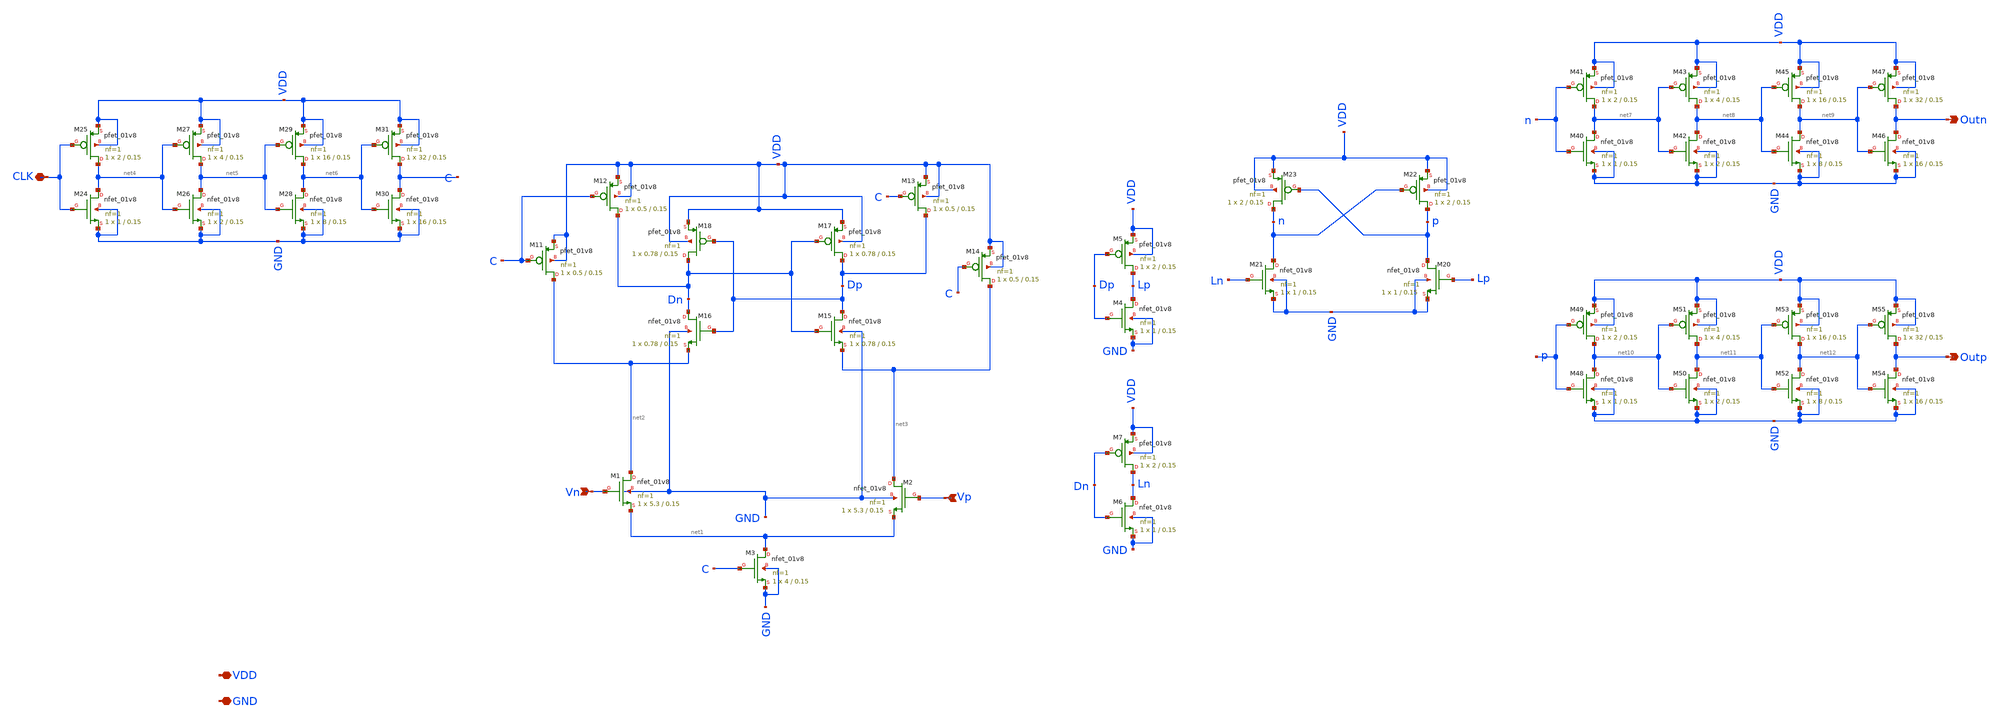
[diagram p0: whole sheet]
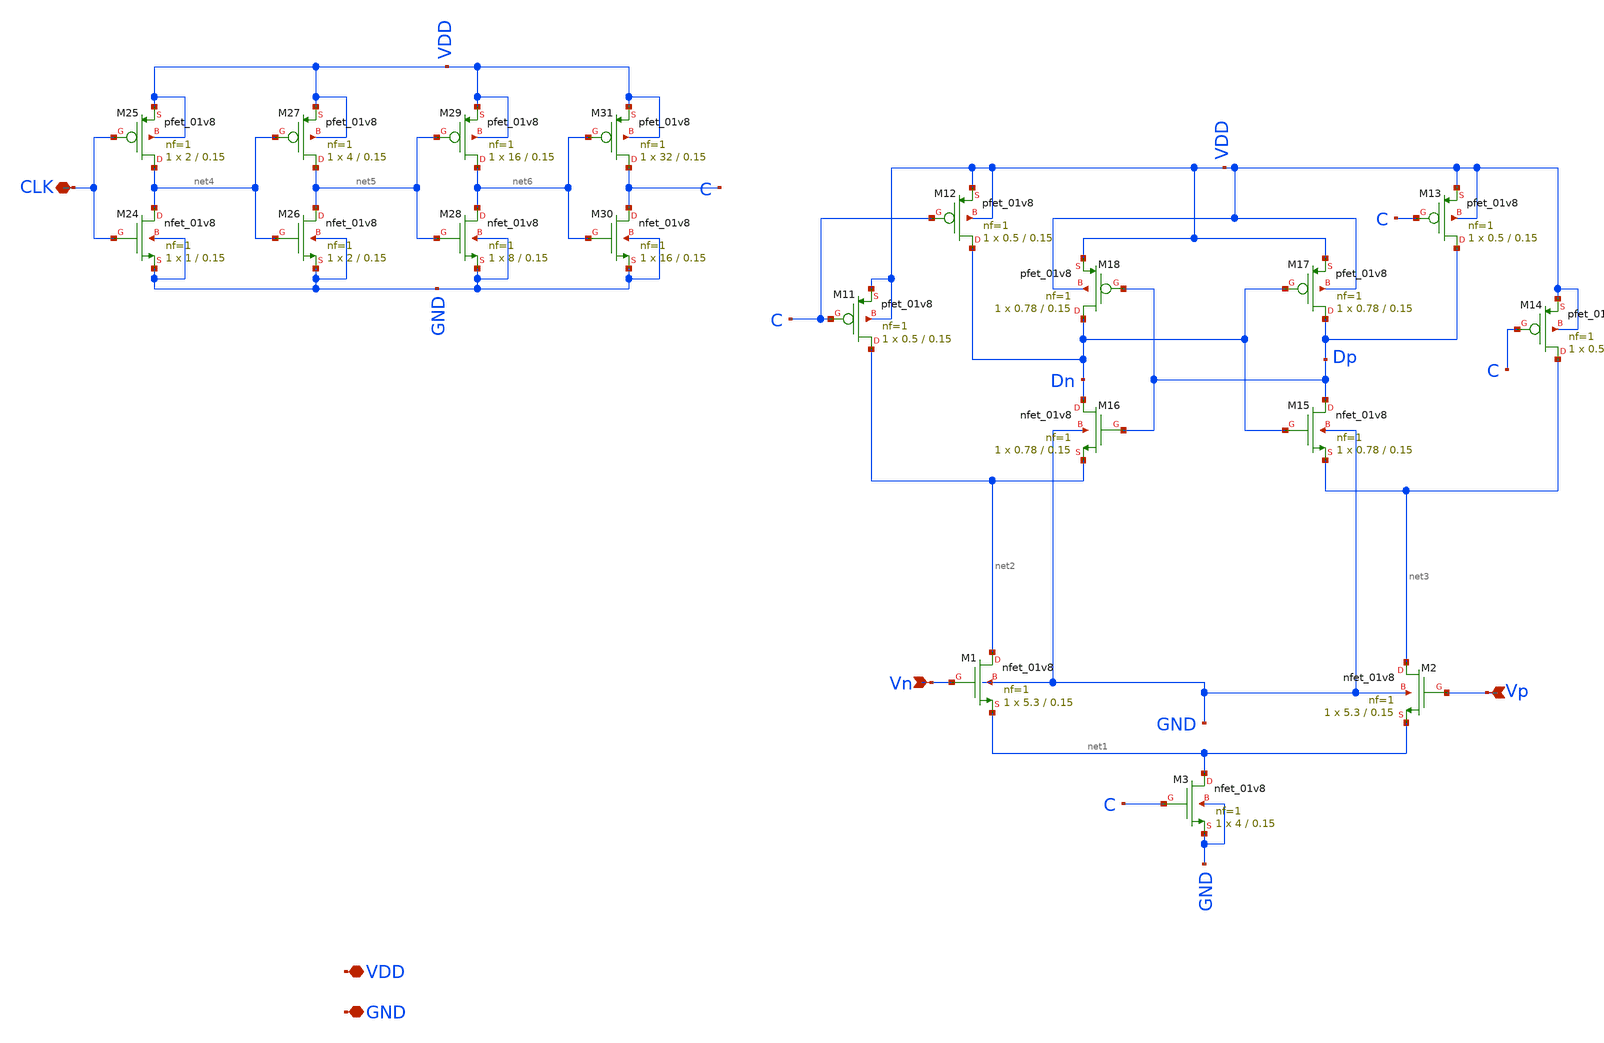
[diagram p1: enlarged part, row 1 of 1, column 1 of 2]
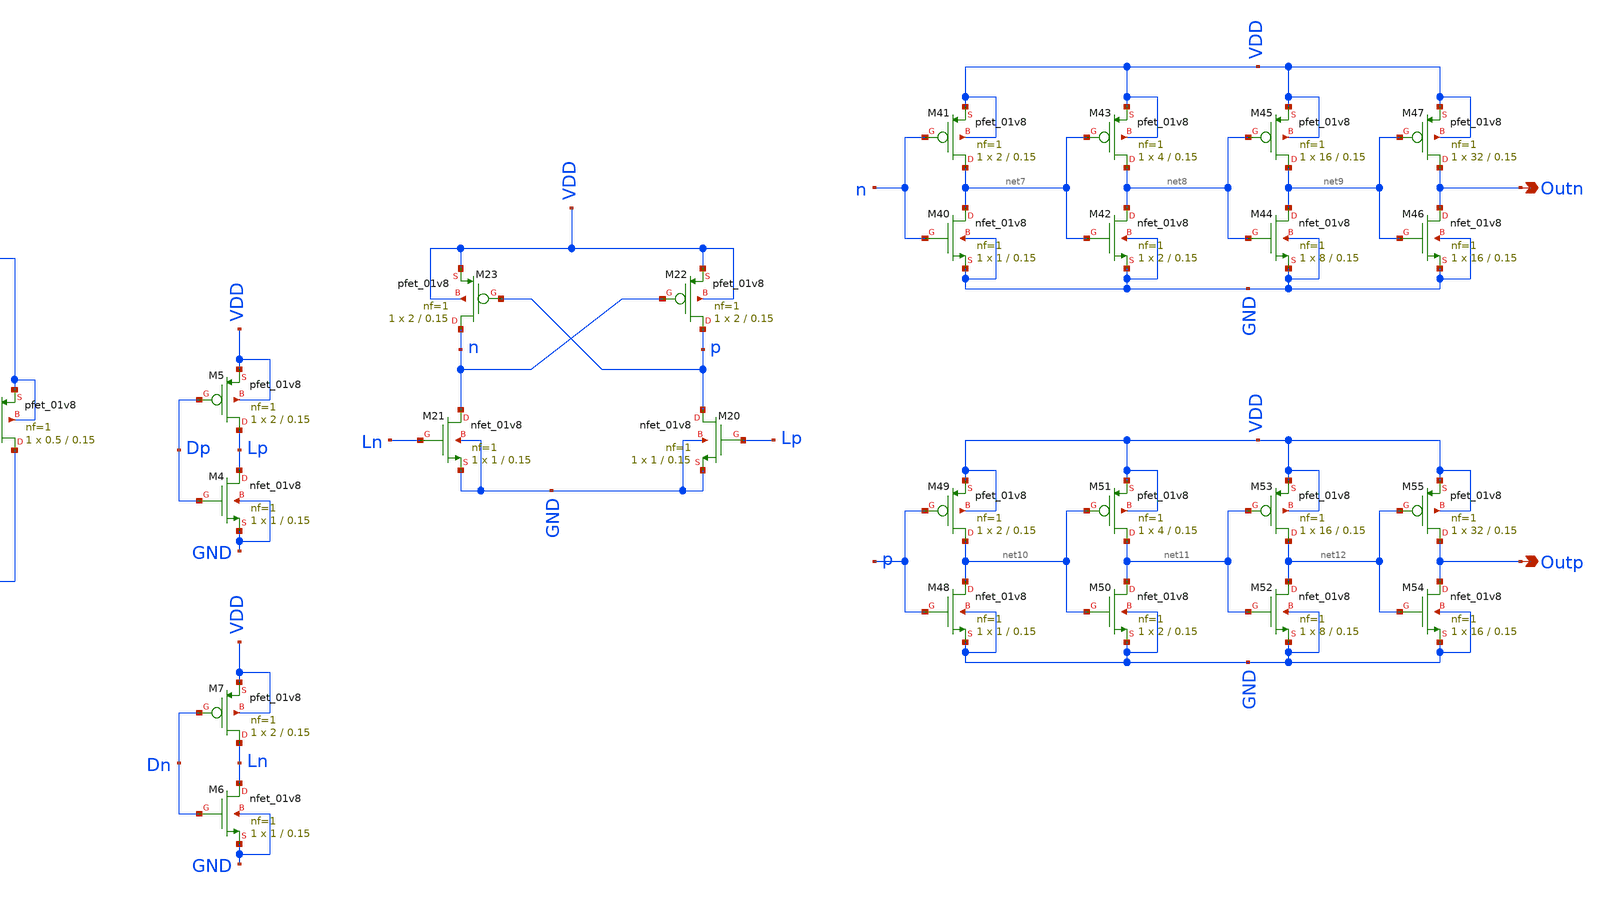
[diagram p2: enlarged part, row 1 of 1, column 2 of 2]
** sch_path: xschem/comparator.sch
**.subckt comparator VDD GND Vp Vn CLK Outn Outp
*.iopin VDD
*.iopin GND
*.ipin Vp
*.ipin Vn
*.iopin CLK
*.opin Outn
*.opin Outp
XM1 net2 Vn net1 GND sky130_fd_pr__nfet_01v8 L=0.15 W=5.3 nf=1 ad='int((nf+1)/2) * W/nf * 0.29' as='int((nf+2)/2) * W/nf * 0.29'
+ pd='2*int((nf+1)/2) * (W/nf + 0.29)' ps='2*int((nf+2)/2) * (W/nf + 0.29)' nrd='0.29 / W' nrs='0.29 / W'
+ sa=0 sb=0 sd=0 mult=1 m=1
XM2 net3 Vp net1 GND sky130_fd_pr__nfet_01v8 L=0.15 W=5.3 nf=1 ad='int((nf+1)/2) * W/nf * 0.29' as='int((nf+2)/2) * W/nf * 0.29'
+ pd='2*int((nf+1)/2) * (W/nf + 0.29)' ps='2*int((nf+2)/2) * (W/nf + 0.29)' nrd='0.29 / W' nrs='0.29 / W'
+ sa=0 sb=0 sd=0 mult=1 m=1
XM3 net1 C GND GND sky130_fd_pr__nfet_01v8 L=0.15 W=4 nf=1 ad='int((nf+1)/2) * W/nf * 0.29' as='int((nf+2)/2) * W/nf * 0.29'
+ pd='2*int((nf+1)/2) * (W/nf + 0.29)' ps='2*int((nf+2)/2) * (W/nf + 0.29)' nrd='0.29 / W' nrs='0.29 / W'
+ sa=0 sb=0 sd=0 mult=1 m=1
XM11 net2 C VDD VDD sky130_fd_pr__pfet_01v8 L=0.15 W=0.5 nf=1 ad='int((nf+1)/2) * W/nf * 0.29' as='int((nf+2)/2) * W/nf * 0.29'
+ pd='2*int((nf+1)/2) * (W/nf + 0.29)' ps='2*int((nf+2)/2) * (W/nf + 0.29)' nrd='0.29 / W' nrs='0.29 / W'
+ sa=0 sb=0 sd=0 mult=1 m=1
XM12 Dn C VDD VDD sky130_fd_pr__pfet_01v8 L=0.15 W=0.5 nf=1 ad='int((nf+1)/2) * W/nf * 0.29' as='int((nf+2)/2) * W/nf * 0.29'
+ pd='2*int((nf+1)/2) * (W/nf + 0.29)' ps='2*int((nf+2)/2) * (W/nf + 0.29)' nrd='0.29 / W' nrs='0.29 / W'
+ sa=0 sb=0 sd=0 mult=1 m=1
XM13 Dp C VDD VDD sky130_fd_pr__pfet_01v8 L=0.15 W=0.5 nf=1 ad='int((nf+1)/2) * W/nf * 0.29' as='int((nf+2)/2) * W/nf * 0.29'
+ pd='2*int((nf+1)/2) * (W/nf + 0.29)' ps='2*int((nf+2)/2) * (W/nf + 0.29)' nrd='0.29 / W' nrs='0.29 / W'
+ sa=0 sb=0 sd=0 mult=1 m=1
XM14 net3 C VDD VDD sky130_fd_pr__pfet_01v8 L=0.15 W=0.5 nf=1 ad='int((nf+1)/2) * W/nf * 0.29' as='int((nf+2)/2) * W/nf * 0.29'
+ pd='2*int((nf+1)/2) * (W/nf + 0.29)' ps='2*int((nf+2)/2) * (W/nf + 0.29)' nrd='0.29 / W' nrs='0.29 / W'
+ sa=0 sb=0 sd=0 mult=1 m=1
XM15 Dp Dn net3 GND sky130_fd_pr__nfet_01v8 L=0.15 W=0.78 nf=1 ad='int((nf+1)/2) * W/nf * 0.29' as='int((nf+2)/2) * W/nf * 0.29'
+ pd='2*int((nf+1)/2) * (W/nf + 0.29)' ps='2*int((nf+2)/2) * (W/nf + 0.29)' nrd='0.29 / W' nrs='0.29 / W'
+ sa=0 sb=0 sd=0 mult=1 m=1
XM16 Dn Dp net2 GND sky130_fd_pr__nfet_01v8 L=0.15 W=0.78 nf=1 ad='int((nf+1)/2) * W/nf * 0.29' as='int((nf+2)/2) * W/nf * 0.29'
+ pd='2*int((nf+1)/2) * (W/nf + 0.29)' ps='2*int((nf+2)/2) * (W/nf + 0.29)' nrd='0.29 / W' nrs='0.29 / W'
+ sa=0 sb=0 sd=0 mult=1 m=1
XM17 Dp Dn VDD VDD sky130_fd_pr__pfet_01v8 L=0.15 W=0.78 nf=1 ad='int((nf+1)/2) * W/nf * 0.29' as='int((nf+2)/2) * W/nf * 0.29'
+ pd='2*int((nf+1)/2) * (W/nf + 0.29)' ps='2*int((nf+2)/2) * (W/nf + 0.29)' nrd='0.29 / W' nrs='0.29 / W'
+ sa=0 sb=0 sd=0 mult=1 m=1
XM18 Dn Dp VDD VDD sky130_fd_pr__pfet_01v8 L=0.15 W=0.78 nf=1 ad='int((nf+1)/2) * W/nf * 0.29' as='int((nf+2)/2) * W/nf * 0.29'
+ pd='2*int((nf+1)/2) * (W/nf + 0.29)' ps='2*int((nf+2)/2) * (W/nf + 0.29)' nrd='0.29 / W' nrs='0.29 / W'
+ sa=0 sb=0 sd=0 mult=1 m=1
XM20 p Lp GND GND sky130_fd_pr__nfet_01v8 L=0.15 W=1 nf=1 ad='int((nf+1)/2) * W/nf * 0.29' as='int((nf+2)/2) * W/nf * 0.29'
+ pd='2*int((nf+1)/2) * (W/nf + 0.29)' ps='2*int((nf+2)/2) * (W/nf + 0.29)' nrd='0.29 / W' nrs='0.29 / W'
+ sa=0 sb=0 sd=0 mult=1 m=1
XM21 n Ln GND GND sky130_fd_pr__nfet_01v8 L=0.15 W=1 nf=1 ad='int((nf+1)/2) * W/nf * 0.29' as='int((nf+2)/2) * W/nf * 0.29'
+ pd='2*int((nf+1)/2) * (W/nf + 0.29)' ps='2*int((nf+2)/2) * (W/nf + 0.29)' nrd='0.29 / W' nrs='0.29 / W'
+ sa=0 sb=0 sd=0 mult=1 m=1
XM22 p n VDD VDD sky130_fd_pr__pfet_01v8 L=0.15 W=2 nf=1 ad='int((nf+1)/2) * W/nf * 0.29' as='int((nf+2)/2) * W/nf * 0.29'
+ pd='2*int((nf+1)/2) * (W/nf + 0.29)' ps='2*int((nf+2)/2) * (W/nf + 0.29)' nrd='0.29 / W' nrs='0.29 / W'
+ sa=0 sb=0 sd=0 mult=1 m=1
XM23 n p VDD VDD sky130_fd_pr__pfet_01v8 L=0.15 W=2 nf=1 ad='int((nf+1)/2) * W/nf * 0.29' as='int((nf+2)/2) * W/nf * 0.29'
+ pd='2*int((nf+1)/2) * (W/nf + 0.29)' ps='2*int((nf+2)/2) * (W/nf + 0.29)' nrd='0.29 / W' nrs='0.29 / W'
+ sa=0 sb=0 sd=0 mult=1 m=1
XM24 net4 CLK GND GND sky130_fd_pr__nfet_01v8 L=0.15 W=1 nf=1 ad='int((nf+1)/2) * W/nf * 0.29' as='int((nf+2)/2) * W/nf * 0.29'
+ pd='2*int((nf+1)/2) * (W/nf + 0.29)' ps='2*int((nf+2)/2) * (W/nf + 0.29)' nrd='0.29 / W' nrs='0.29 / W'
+ sa=0 sb=0 sd=0 mult=1 m=1
XM25 net4 CLK VDD VDD sky130_fd_pr__pfet_01v8 L=0.15 W=2 nf=1 ad='int((nf+1)/2) * W/nf * 0.29' as='int((nf+2)/2) * W/nf * 0.29'
+ pd='2*int((nf+1)/2) * (W/nf + 0.29)' ps='2*int((nf+2)/2) * (W/nf + 0.29)' nrd='0.29 / W' nrs='0.29 / W'
+ sa=0 sb=0 sd=0 mult=1 m=1
XM26 net5 net4 GND GND sky130_fd_pr__nfet_01v8 L=0.15 W=2 nf=1 ad='int((nf+1)/2) * W/nf * 0.29' as='int((nf+2)/2) * W/nf * 0.29'
+ pd='2*int((nf+1)/2) * (W/nf + 0.29)' ps='2*int((nf+2)/2) * (W/nf + 0.29)' nrd='0.29 / W' nrs='0.29 / W'
+ sa=0 sb=0 sd=0 mult=1 m=1
XM27 net5 net4 VDD VDD sky130_fd_pr__pfet_01v8 L=0.15 W=4 nf=1 ad='int((nf+1)/2) * W/nf * 0.29' as='int((nf+2)/2) * W/nf * 0.29'
+ pd='2*int((nf+1)/2) * (W/nf + 0.29)' ps='2*int((nf+2)/2) * (W/nf + 0.29)' nrd='0.29 / W' nrs='0.29 / W'
+ sa=0 sb=0 sd=0 mult=1 m=1
XM28 net6 net5 GND GND sky130_fd_pr__nfet_01v8 L=0.15 W=8 nf=1 ad='int((nf+1)/2) * W/nf * 0.29' as='int((nf+2)/2) * W/nf * 0.29'
+ pd='2*int((nf+1)/2) * (W/nf + 0.29)' ps='2*int((nf+2)/2) * (W/nf + 0.29)' nrd='0.29 / W' nrs='0.29 / W'
+ sa=0 sb=0 sd=0 mult=1 m=1
XM29 net6 net5 VDD VDD sky130_fd_pr__pfet_01v8 L=0.15 W=16 nf=1 ad='int((nf+1)/2) * W/nf * 0.29' as='int((nf+2)/2) * W/nf * 0.29'
+ pd='2*int((nf+1)/2) * (W/nf + 0.29)' ps='2*int((nf+2)/2) * (W/nf + 0.29)' nrd='0.29 / W' nrs='0.29 / W'
+ sa=0 sb=0 sd=0 mult=1 m=1
XM30 C net6 GND GND sky130_fd_pr__nfet_01v8 L=0.15 W=16 nf=1 ad='int((nf+1)/2) * W/nf * 0.29' as='int((nf+2)/2) * W/nf * 0.29'
+ pd='2*int((nf+1)/2) * (W/nf + 0.29)' ps='2*int((nf+2)/2) * (W/nf + 0.29)' nrd='0.29 / W' nrs='0.29 / W'
+ sa=0 sb=0 sd=0 mult=1 m=1
XM31 C net6 VDD VDD sky130_fd_pr__pfet_01v8 L=0.15 W=32 nf=1 ad='int((nf+1)/2) * W/nf * 0.29' as='int((nf+2)/2) * W/nf * 0.29'
+ pd='2*int((nf+1)/2) * (W/nf + 0.29)' ps='2*int((nf+2)/2) * (W/nf + 0.29)' nrd='0.29 / W' nrs='0.29 / W'
+ sa=0 sb=0 sd=0 mult=1 m=1
XM40 net7 n GND GND sky130_fd_pr__nfet_01v8 L=0.15 W=1 nf=1 ad='int((nf+1)/2) * W/nf * 0.29' as='int((nf+2)/2) * W/nf * 0.29'
+ pd='2*int((nf+1)/2) * (W/nf + 0.29)' ps='2*int((nf+2)/2) * (W/nf + 0.29)' nrd='0.29 / W' nrs='0.29 / W'
+ sa=0 sb=0 sd=0 mult=1 m=1
XM41 net7 n VDD VDD sky130_fd_pr__pfet_01v8 L=0.15 W=2 nf=1 ad='int((nf+1)/2) * W/nf * 0.29' as='int((nf+2)/2) * W/nf * 0.29'
+ pd='2*int((nf+1)/2) * (W/nf + 0.29)' ps='2*int((nf+2)/2) * (W/nf + 0.29)' nrd='0.29 / W' nrs='0.29 / W'
+ sa=0 sb=0 sd=0 mult=1 m=1
XM42 net8 net7 GND GND sky130_fd_pr__nfet_01v8 L=0.15 W=2 nf=1 ad='int((nf+1)/2) * W/nf * 0.29' as='int((nf+2)/2) * W/nf * 0.29'
+ pd='2*int((nf+1)/2) * (W/nf + 0.29)' ps='2*int((nf+2)/2) * (W/nf + 0.29)' nrd='0.29 / W' nrs='0.29 / W'
+ sa=0 sb=0 sd=0 mult=1 m=1
XM43 net8 net7 VDD VDD sky130_fd_pr__pfet_01v8 L=0.15 W=4 nf=1 ad='int((nf+1)/2) * W/nf * 0.29' as='int((nf+2)/2) * W/nf * 0.29'
+ pd='2*int((nf+1)/2) * (W/nf + 0.29)' ps='2*int((nf+2)/2) * (W/nf + 0.29)' nrd='0.29 / W' nrs='0.29 / W'
+ sa=0 sb=0 sd=0 mult=1 m=1
XM44 net9 net8 GND GND sky130_fd_pr__nfet_01v8 L=0.15 W=8 nf=1 ad='int((nf+1)/2) * W/nf * 0.29' as='int((nf+2)/2) * W/nf * 0.29'
+ pd='2*int((nf+1)/2) * (W/nf + 0.29)' ps='2*int((nf+2)/2) * (W/nf + 0.29)' nrd='0.29 / W' nrs='0.29 / W'
+ sa=0 sb=0 sd=0 mult=1 m=1
XM45 net9 net8 VDD VDD sky130_fd_pr__pfet_01v8 L=0.15 W=16 nf=1 ad='int((nf+1)/2) * W/nf * 0.29' as='int((nf+2)/2) * W/nf * 0.29'
+ pd='2*int((nf+1)/2) * (W/nf + 0.29)' ps='2*int((nf+2)/2) * (W/nf + 0.29)' nrd='0.29 / W' nrs='0.29 / W'
+ sa=0 sb=0 sd=0 mult=1 m=1
XM46 Outn net9 GND GND sky130_fd_pr__nfet_01v8 L=0.15 W=16 nf=1 ad='int((nf+1)/2) * W/nf * 0.29' as='int((nf+2)/2) * W/nf * 0.29'
+ pd='2*int((nf+1)/2) * (W/nf + 0.29)' ps='2*int((nf+2)/2) * (W/nf + 0.29)' nrd='0.29 / W' nrs='0.29 / W'
+ sa=0 sb=0 sd=0 mult=1 m=1
XM47 Outn net9 VDD VDD sky130_fd_pr__pfet_01v8 L=0.15 W=32 nf=1 ad='int((nf+1)/2) * W/nf * 0.29' as='int((nf+2)/2) * W/nf * 0.29'
+ pd='2*int((nf+1)/2) * (W/nf + 0.29)' ps='2*int((nf+2)/2) * (W/nf + 0.29)' nrd='0.29 / W' nrs='0.29 / W'
+ sa=0 sb=0 sd=0 mult=1 m=1
XM48 net10 p GND GND sky130_fd_pr__nfet_01v8 L=0.15 W=1 nf=1 ad='int((nf+1)/2) * W/nf * 0.29' as='int((nf+2)/2) * W/nf * 0.29'
+ pd='2*int((nf+1)/2) * (W/nf + 0.29)' ps='2*int((nf+2)/2) * (W/nf + 0.29)' nrd='0.29 / W' nrs='0.29 / W'
+ sa=0 sb=0 sd=0 mult=1 m=1
XM49 net10 p VDD VDD sky130_fd_pr__pfet_01v8 L=0.15 W=2 nf=1 ad='int((nf+1)/2) * W/nf * 0.29' as='int((nf+2)/2) * W/nf * 0.29'
+ pd='2*int((nf+1)/2) * (W/nf + 0.29)' ps='2*int((nf+2)/2) * (W/nf + 0.29)' nrd='0.29 / W' nrs='0.29 / W'
+ sa=0 sb=0 sd=0 mult=1 m=1
XM50 net11 net10 GND GND sky130_fd_pr__nfet_01v8 L=0.15 W=2 nf=1 ad='int((nf+1)/2) * W/nf * 0.29' as='int((nf+2)/2) * W/nf * 0.29'
+ pd='2*int((nf+1)/2) * (W/nf + 0.29)' ps='2*int((nf+2)/2) * (W/nf + 0.29)' nrd='0.29 / W' nrs='0.29 / W'
+ sa=0 sb=0 sd=0 mult=1 m=1
XM51 net11 net10 VDD VDD sky130_fd_pr__pfet_01v8 L=0.15 W=4 nf=1 ad='int((nf+1)/2) * W/nf * 0.29' as='int((nf+2)/2) * W/nf * 0.29'
+ pd='2*int((nf+1)/2) * (W/nf + 0.29)' ps='2*int((nf+2)/2) * (W/nf + 0.29)' nrd='0.29 / W' nrs='0.29 / W'
+ sa=0 sb=0 sd=0 mult=1 m=1
XM52 net12 net11 GND GND sky130_fd_pr__nfet_01v8 L=0.15 W=8 nf=1 ad='int((nf+1)/2) * W/nf * 0.29' as='int((nf+2)/2) * W/nf * 0.29'
+ pd='2*int((nf+1)/2) * (W/nf + 0.29)' ps='2*int((nf+2)/2) * (W/nf + 0.29)' nrd='0.29 / W' nrs='0.29 / W'
+ sa=0 sb=0 sd=0 mult=1 m=1
XM53 net12 net11 VDD VDD sky130_fd_pr__pfet_01v8 L=0.15 W=16 nf=1 ad='int((nf+1)/2) * W/nf * 0.29' as='int((nf+2)/2) * W/nf * 0.29'
+ pd='2*int((nf+1)/2) * (W/nf + 0.29)' ps='2*int((nf+2)/2) * (W/nf + 0.29)' nrd='0.29 / W' nrs='0.29 / W'
+ sa=0 sb=0 sd=0 mult=1 m=1
XM54 Outp net12 GND GND sky130_fd_pr__nfet_01v8 L=0.15 W=16 nf=1 ad='int((nf+1)/2) * W/nf * 0.29' as='int((nf+2)/2) * W/nf * 0.29'
+ pd='2*int((nf+1)/2) * (W/nf + 0.29)' ps='2*int((nf+2)/2) * (W/nf + 0.29)' nrd='0.29 / W' nrs='0.29 / W'
+ sa=0 sb=0 sd=0 mult=1 m=1
XM55 Outp net12 VDD VDD sky130_fd_pr__pfet_01v8 L=0.15 W=32 nf=1 ad='int((nf+1)/2) * W/nf * 0.29' as='int((nf+2)/2) * W/nf * 0.29'
+ pd='2*int((nf+1)/2) * (W/nf + 0.29)' ps='2*int((nf+2)/2) * (W/nf + 0.29)' nrd='0.29 / W' nrs='0.29 / W'
+ sa=0 sb=0 sd=0 mult=1 m=1
XM4 Lp Dp GND GND sky130_fd_pr__nfet_01v8 L=0.15 W=1 nf=1 ad='int((nf+1)/2) * W/nf * 0.29' as='int((nf+2)/2) * W/nf * 0.29'
+ pd='2*int((nf+1)/2) * (W/nf + 0.29)' ps='2*int((nf+2)/2) * (W/nf + 0.29)' nrd='0.29 / W' nrs='0.29 / W'
+ sa=0 sb=0 sd=0 mult=1 m=1
XM5 Lp Dp VDD VDD sky130_fd_pr__pfet_01v8 L=0.15 W=2 nf=1 ad='int((nf+1)/2) * W/nf * 0.29' as='int((nf+2)/2) * W/nf * 0.29'
+ pd='2*int((nf+1)/2) * (W/nf + 0.29)' ps='2*int((nf+2)/2) * (W/nf + 0.29)' nrd='0.29 / W' nrs='0.29 / W'
+ sa=0 sb=0 sd=0 mult=1 m=1
XM6 Ln Dn GND GND sky130_fd_pr__nfet_01v8 L=0.15 W=1 nf=1 ad='int((nf+1)/2) * W/nf * 0.29' as='int((nf+2)/2) * W/nf * 0.29'
+ pd='2*int((nf+1)/2) * (W/nf + 0.29)' ps='2*int((nf+2)/2) * (W/nf + 0.29)' nrd='0.29 / W' nrs='0.29 / W'
+ sa=0 sb=0 sd=0 mult=1 m=1
XM7 Ln Dn VDD VDD sky130_fd_pr__pfet_01v8 L=0.15 W=2 nf=1 ad='int((nf+1)/2) * W/nf * 0.29' as='int((nf+2)/2) * W/nf * 0.29'
+ pd='2*int((nf+1)/2) * (W/nf + 0.29)' ps='2*int((nf+2)/2) * (W/nf + 0.29)' nrd='0.29 / W' nrs='0.29 / W'
+ sa=0 sb=0 sd=0 mult=1 m=1
**.ends
.end
